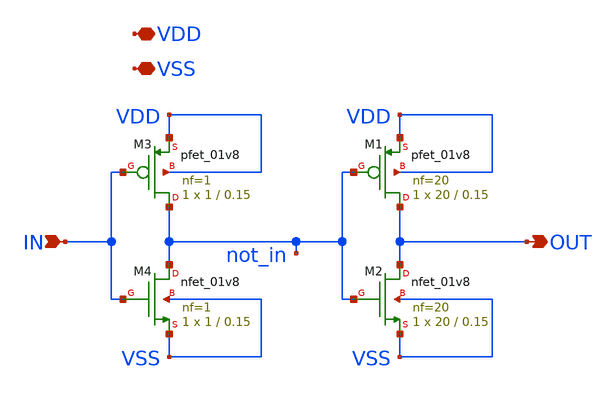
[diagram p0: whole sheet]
** sch_path: xschem/inverter.sch
**.subckt inverter VDD VSS IN OUT
*.iopin VDD
*.iopin VSS
*.ipin IN
*.opin OUT
XM1 OUT not_in VDD VDD sky130_fd_pr__pfet_01v8 L=0.15 W=20 nf=20 ad='int((nf+1)/2) * W/nf * 0.29' as='int((nf+2)/2) * W/nf * 0.29'
+ pd='2*int((nf+1)/2) * (W/nf + 0.29)' ps='2*int((nf+2)/2) * (W/nf + 0.29)' nrd='0.29 / W' nrs='0.29 / W'
+ sa=0 sb=0 sd=0 mult=1 m=1
XM2 OUT not_in VSS VSS sky130_fd_pr__nfet_01v8 L=0.15 W=20 nf=20 ad='int((nf+1)/2) * W/nf * 0.29' as='int((nf+2)/2) * W/nf * 0.29'
+ pd='2*int((nf+1)/2) * (W/nf + 0.29)' ps='2*int((nf+2)/2) * (W/nf + 0.29)' nrd='0.29 / W' nrs='0.29 / W'
+ sa=0 sb=0 sd=0 mult=1 m=1
XM3 not_in IN VDD VDD sky130_fd_pr__pfet_01v8 L=0.15 W=1 nf=1 ad='int((nf+1)/2) * W/nf * 0.29' as='int((nf+2)/2) * W/nf * 0.29'
+ pd='2*int((nf+1)/2) * (W/nf + 0.29)' ps='2*int((nf+2)/2) * (W/nf + 0.29)' nrd='0.29 / W' nrs='0.29 / W'
+ sa=0 sb=0 sd=0 mult=1 m=1
XM4 not_in IN VSS VSS sky130_fd_pr__nfet_01v8 L=0.15 W=1 nf=1 ad='int((nf+1)/2) * W/nf * 0.29' as='int((nf+2)/2) * W/nf * 0.29'
+ pd='2*int((nf+1)/2) * (W/nf + 0.29)' ps='2*int((nf+2)/2) * (W/nf + 0.29)' nrd='0.29 / W' nrs='0.29 / W'
+ sa=0 sb=0 sd=0 mult=1 m=1
**.ends
.end
